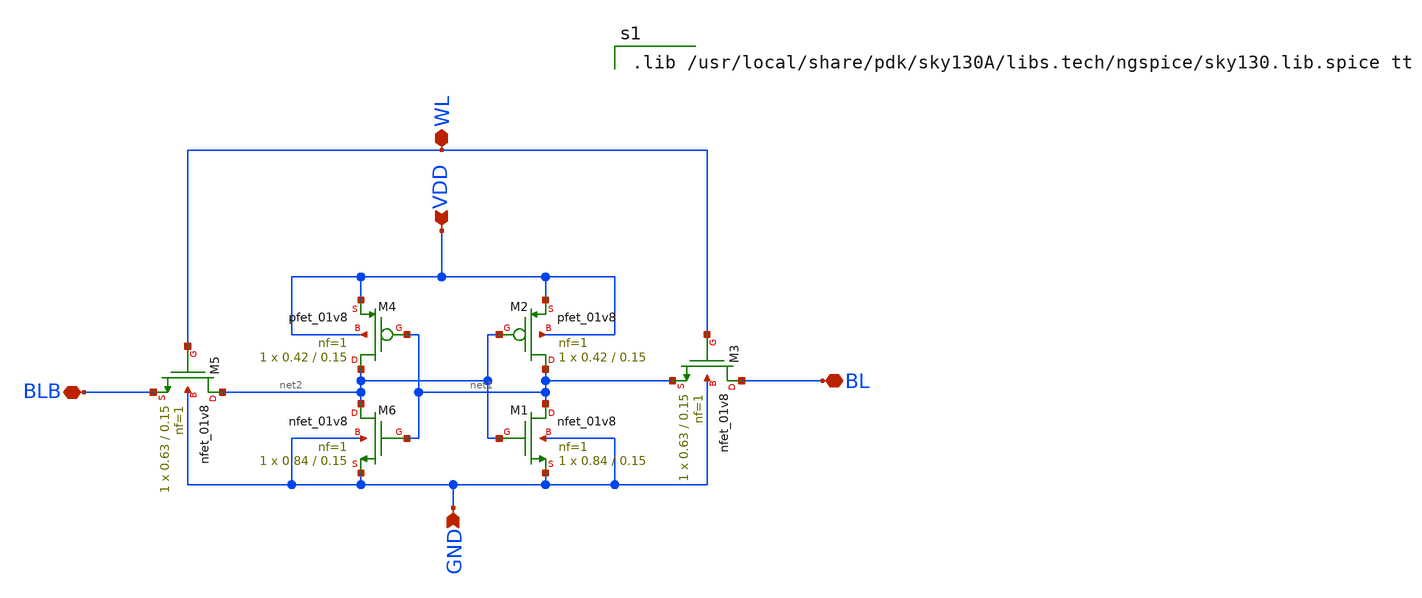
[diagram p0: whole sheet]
** sch_path: schematics/schematics.sch
**.subckt schematics BL VDD GND BLB WL
*.iopin BL
*.ipin VDD
*.ipin GND
*.iopin BLB
*.iopin WL
XM2 net1 net2 VDD VDD sky130_fd_pr__pfet_01v8 L=0.15 W=0.42 nf=1 ad='int((1 + 1)/2) * 0.42 / 1 * 0.29'
+ as='int((1 + 2)/2) * 0.42 / 1 * 0.29' pd='2*int((1 + 1)/2) * (0.42 / 1 + 0.29)' ps='2*int((1 + 2)/2) * (0.42 / 1 + 0.29)'
+ nrd='0.29 / 0.42 ' nrs='0.29 / 0.42 ' sa=0 sb=0 sd=0 mult=1 m=1
XM4 net2 net1 VDD VDD sky130_fd_pr__pfet_01v8 L=0.15 W=0.42 nf=1 ad='int((1 + 1)/2) * 0.42 / 1 * 0.29'
+ as='int((1 + 2)/2) * 0.42 / 1 * 0.29' pd='2*int((1 + 1)/2) * (0.42 / 1 + 0.29)' ps='2*int((1 + 2)/2) * (0.42 / 1 + 0.29)'
+ nrd='0.29 / 0.42 ' nrs='0.29 / 0.42 ' sa=0 sb=0 sd=0 mult=1 m=1
XM1 net1 net2 GND GND sky130_fd_pr__nfet_01v8 L=0.15 W=0.84 nf=1 ad='int((1 + 1)/2) * 0.84 / 1 * 0.29'
+ as='int((1 + 2)/2) * 0.84 / 1 * 0.29' pd='2*int((1 + 1)/2) * (0.84 / 1 + 0.29)' ps='2*int((1 + 2)/2) * (0.84 / 1 + 0.29)'
+ nrd='0.29 / 0.84 ' nrs='0.29 / 0.84 ' sa=0 sb=0 sd=0 mult=1 m=1
XM3 BL WL net1 GND sky130_fd_pr__nfet_01v8 L=0.15 W=0.63 nf=1 ad='int((1 + 1)/2) * 0.63 / 1 * 0.29' as='int((1 + 2)/2) * 0.63 / 1 * 0.29'
+ pd='2*int((1 + 1)/2) * (0.63 / 1 + 0.29)' ps='2*int((1 + 2)/2) * (0.63 / 1 + 0.29)' nrd='0.29 / 0.63 '
+ nrs='0.29 / 0.63 ' sa=0 sb=0 sd=0 mult=1 m=1
XM5 net2 WL BLB GND sky130_fd_pr__nfet_01v8 L=0.15 W=0.63 nf=1 ad='int((1 + 1)/2) * 0.63 / 1 * 0.29'
+ as='int((1 + 2)/2) * 0.63 / 1 * 0.29' pd='2*int((1 + 1)/2) * (0.63 / 1 + 0.29)' ps='2*int((1 + 2)/2) * (0.63 / 1 + 0.29)'
+ nrd='0.29 / 0.63 ' nrs='0.29 / 0.63 ' sa=0 sb=0 sd=0 mult=1 m=1
XM6 net2 net1 GND GND sky130_fd_pr__nfet_01v8 L=0.15 W=0.84 nf=1 ad='int((1 + 1)/2) * 0.84 / 1 * 0.29'
+ as='int((1 + 2)/2) * 0.84 / 1 * 0.29' pd='2*int((1 + 1)/2) * (0.84 / 1 + 0.29)' ps='2*int((1 + 2)/2) * (0.84 / 1 + 0.29)'
+ nrd='0.29 / 0.84 ' nrs='0.29 / 0.84 ' sa=0 sb=0 sd=0 mult=1 m=1
**** begin user architecture code

.lib /usr/local/share/pdk/sky130A/libs.tech/ngspice/sky130.lib.spice tt

**** end user architecture code
**.ends
.end
